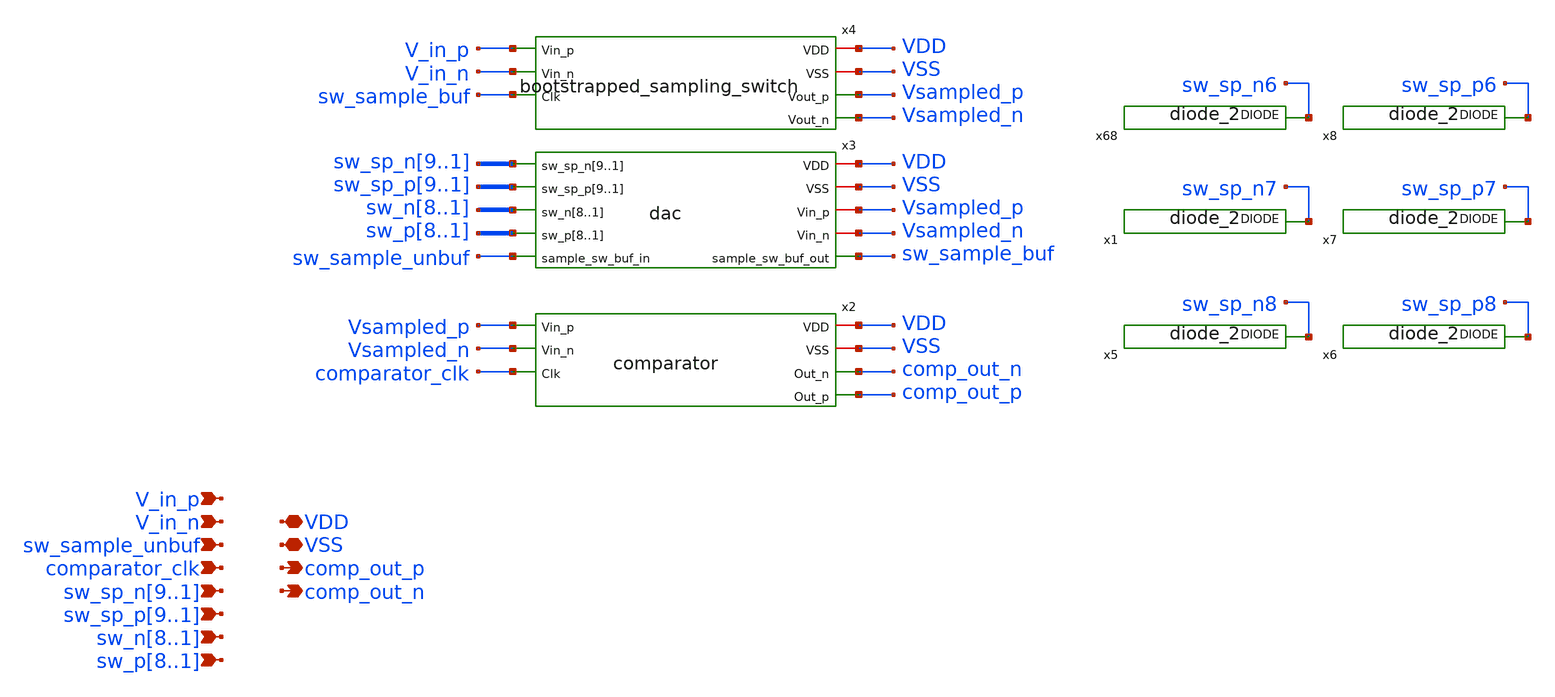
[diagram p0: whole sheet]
** sch_path: xschem/src/all_analog/all_analog.sch
**.subckt all_analog VDD V_in_p VSS V_in_n comp_out_p sw_sample_unbuf comparator_clk
*+ sw_sp_n9,sw_sp_n8,sw_sp_n7,sw_sp_n6,sw_sp_n5,sw_sp_n4,sw_sp_n3,sw_sp_n2,sw_sp_n1 sw_sp_p9,sw_sp_p8,sw_sp_p7,sw_sp_p6,sw_sp_p5,sw_sp_p4,sw_sp_p3,sw_sp_p2,sw_sp_p1
*+ sw_n8,sw_n7,sw_n6,sw_n5,sw_n4,sw_n3,sw_n2,sw_n1 sw_p8,sw_p7,sw_p6,sw_p5,sw_p4,sw_p3,sw_p2,sw_p1 comp_out_n
*.iopin VDD
*.ipin V_in_p
*.iopin VSS
*.ipin V_in_n
*.opin comp_out_p
*.ipin sw_sample_unbuf
*.ipin comparator_clk
*.ipin sw_sp_n9,sw_sp_n8,sw_sp_n7,sw_sp_n6,sw_sp_n5,sw_sp_n4,sw_sp_n3,sw_sp_n2,sw_sp_n1
*.ipin sw_sp_p9,sw_sp_p8,sw_sp_p7,sw_sp_p6,sw_sp_p5,sw_sp_p4,sw_sp_p3,sw_sp_p2,sw_sp_p1
*.ipin sw_n8,sw_n7,sw_n6,sw_n5,sw_n4,sw_n3,sw_n2,sw_n1
*.ipin sw_p8,sw_p7,sw_p6,sw_p5,sw_p4,sw_p3,sw_p2,sw_p1
*.opin comp_out_n
x3 sw_sp_n9 sw_sp_n8 sw_sp_n7 sw_sp_n6 sw_sp_n5 sw_sp_n4 sw_sp_n3 sw_sp_n2 sw_sp_n1 VDD sw_sp_p9
+ sw_sp_p8 sw_sp_p7 sw_sp_p6 sw_sp_p5 sw_sp_p4 sw_sp_p3 sw_sp_p2 sw_sp_p1 VSS sw_n8 sw_n7 sw_n6 sw_n5 sw_n4
+ sw_n3 sw_n2 sw_n1 Vsampled_p Vsampled_n sw_p8 sw_p7 sw_p6 sw_p5 sw_p4 sw_p3 sw_p2 sw_p1 sw_sample_buf
+ sw_sample_unbuf dac
x4 VDD V_in_p VSS V_in_n sw_sample_buf Vsampled_p Vsampled_n bootstrapped_sampling_switch
x2 VDD VSS Vsampled_p comp_out_n Vsampled_n comp_out_p comparator_clk comparator
x68 sw_sp_n6 VSS VSS VDD VDD sky130_fd_sc_hd__diode_2
x1 sw_sp_n7 VSS VSS VDD VDD sky130_fd_sc_hd__diode_2
x5 sw_sp_n8 VSS VSS VDD VDD sky130_fd_sc_hd__diode_2
x6 sw_sp_p8 VSS VSS VDD VDD sky130_fd_sc_hd__diode_2
x7 sw_sp_p7 VSS VSS VDD VDD sky130_fd_sc_hd__diode_2
x8 sw_sp_p6 VSS VSS VDD VDD sky130_fd_sc_hd__diode_2
**** begin user architecture code
 *.lib $::SKYWATER_MODELS/sky130.lib.spice tt
.include $::SKYWATER_STDCELLS/sky130_fd_sc_hd.spice

**** end user architecture code
**.ends
.end
